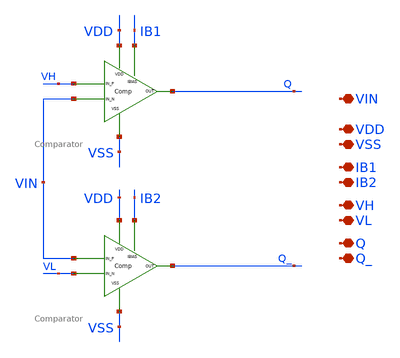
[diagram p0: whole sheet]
** sch_path: xschem/DC_DC_Converter_xschem/OTHERS/DC_DC_Converter_JV9/Comparator_Pair/cmp_pair.sch
**.subckt cmp_pair VDD VSS IB1 IB2 VH VL Q Q_ VIN
*.iopin VDD
*.iopin VSS
*.iopin IB1
*.iopin IB2
*.iopin VH
*.iopin VL
*.iopin Q
*.iopin Q_
*.iopin VIN
XM1 IB1 VDD VH VIN VSS Q Comparator
XM2 IB2 VDD VIN VL VSS Q_ Comparator
**.ends
.end
